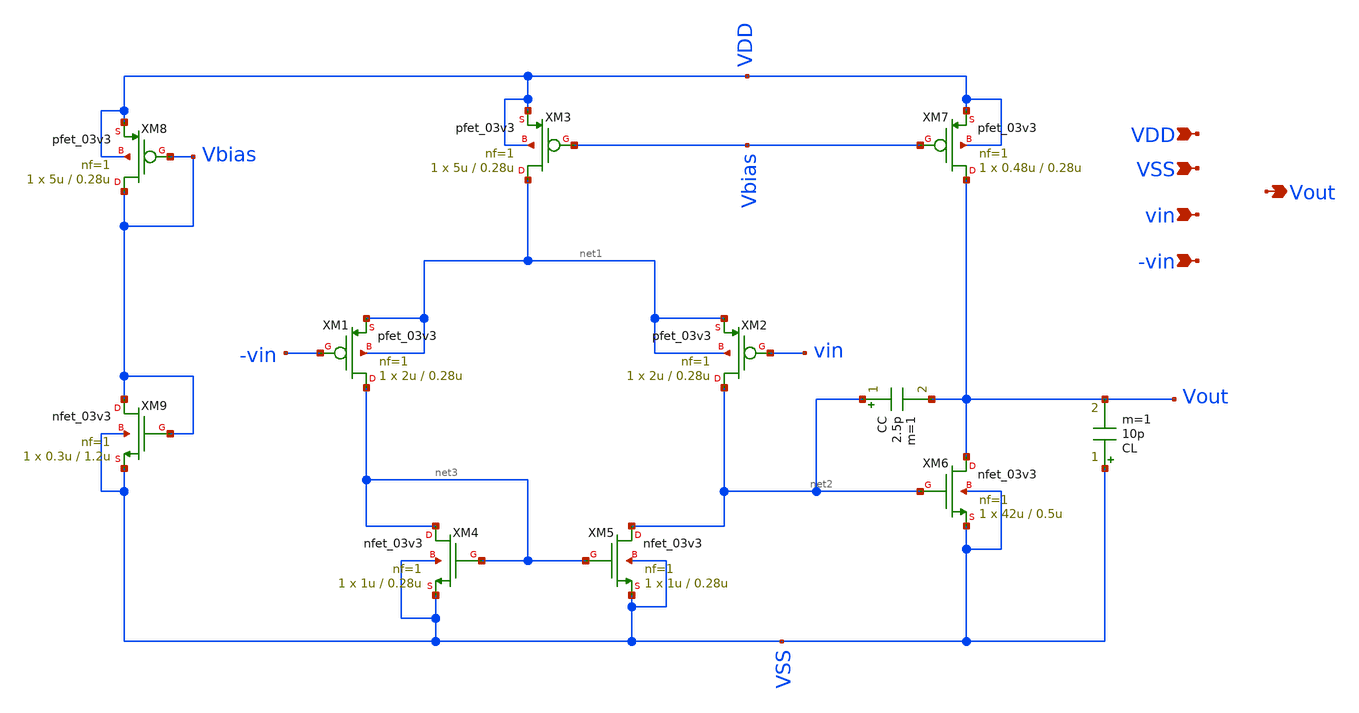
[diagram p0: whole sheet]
** sch_path: designs/First cut design/pmosipdiffpairopamp.sch
**.subckt pmosipdiffpairopamp VDD VSS vin -vin Vout
*.ipin VDD
*.ipin VSS
*.ipin vin
*.ipin -vin
*.opin Vout
XM1 net3 -vin net1 net1 pfet_03v3 L=0.28u W=2u nf=1 ad='int((nf+1)/2) * W/nf * 0.18u' as='int((nf+2)/2) * W/nf * 0.18u'
+ pd='2*int((nf+1)/2) * (W/nf + 0.18u)' ps='2*int((nf+2)/2) * (W/nf + 0.18u)' nrd='0.18u / W' nrs='0.18u / W'
+ sa=0 sb=0 sd=0 m=1
XM2 net2 vin net1 net1 pfet_03v3 L=0.28u W=2u nf=1 ad='int((nf+1)/2) * W/nf * 0.18u' as='int((nf+2)/2) * W/nf * 0.18u'
+ pd='2*int((nf+1)/2) * (W/nf + 0.18u)' ps='2*int((nf+2)/2) * (W/nf + 0.18u)' nrd='0.18u / W' nrs='0.18u / W'
+ sa=0 sb=0 sd=0 m=1
XM3 net1 Vbias VDD VDD pfet_03v3 L=0.28u W=5u nf=1 ad='int((nf+1)/2) * W/nf * 0.18u' as='int((nf+2)/2) * W/nf * 0.18u'
+ pd='2*int((nf+1)/2) * (W/nf + 0.18u)' ps='2*int((nf+2)/2) * (W/nf + 0.18u)' nrd='0.18u / W' nrs='0.18u / W'
+ sa=0 sb=0 sd=0 m=1
XM4 net3 net3 VSS VSS nfet_03v3 L=0.28u W=1u nf=1 ad='int((nf+1)/2) * W/nf * 0.18u' as='int((nf+2)/2) * W/nf * 0.18u'
+ pd='2*int((nf+1)/2) * (W/nf + 0.18u)' ps='2*int((nf+2)/2) * (W/nf + 0.18u)' nrd='0.18u / W' nrs='0.18u / W'
+ sa=0 sb=0 sd=0 m=1
XM5 net2 net3 VSS VSS nfet_03v3 L=0.28u W=1u nf=1 ad='int((nf+1)/2) * W/nf * 0.18u' as='int((nf+2)/2) * W/nf * 0.18u'
+ pd='2*int((nf+1)/2) * (W/nf + 0.18u)' ps='2*int((nf+2)/2) * (W/nf + 0.18u)' nrd='0.18u / W' nrs='0.18u / W'
+ sa=0 sb=0 sd=0 m=1
XM6 Vout net2 VSS VSS nfet_03v3 L=0.5u W=42u nf=1 ad='int((nf+1)/2) * W/nf * 0.18u' as='int((nf+2)/2) * W/nf * 0.18u'
+ pd='2*int((nf+1)/2) * (W/nf + 0.18u)' ps='2*int((nf+2)/2) * (W/nf + 0.18u)' nrd='0.18u / W' nrs='0.18u / W'
+ sa=0 sb=0 sd=0 m=1
XM7 Vout Vbias VDD VDD pfet_03v3 L=0.28u W=0.48u nf=1 ad='int((nf+1)/2) * W/nf * 0.18u' as='int((nf+2)/2) * W/nf * 0.18u'
+ pd='2*int((nf+1)/2) * (W/nf + 0.18u)' ps='2*int((nf+2)/2) * (W/nf + 0.18u)' nrd='0.18u / W' nrs='0.18u / W'
+ sa=0 sb=0 sd=0 m=1
CC net2 Vout 2.5p m=1
CL VSS Vout 10p m=1
XM8 Vbias Vbias VDD VDD pfet_03v3 L=0.28u W=5u nf=1 ad='int((nf+1)/2) * W/nf * 0.18u' as='int((nf+2)/2) * W/nf * 0.18u'
+ pd='2*int((nf+1)/2) * (W/nf + 0.18u)' ps='2*int((nf+2)/2) * (W/nf + 0.18u)' nrd='0.18u / W' nrs='0.18u / W'
+ sa=0 sb=0 sd=0 m=1
XM9 Vbias Vbias VSS VSS nfet_03v3 L=1.2u W=0.3u nf=1 ad='int((nf+1)/2) * W/nf * 0.18u' as='int((nf+2)/2) * W/nf * 0.18u'
+ pd='2*int((nf+1)/2) * (W/nf + 0.18u)' ps='2*int((nf+2)/2) * (W/nf + 0.18u)' nrd='0.18u / W' nrs='0.18u / W'
+ sa=0 sb=0 sd=0 m=1
**.ends
.end
